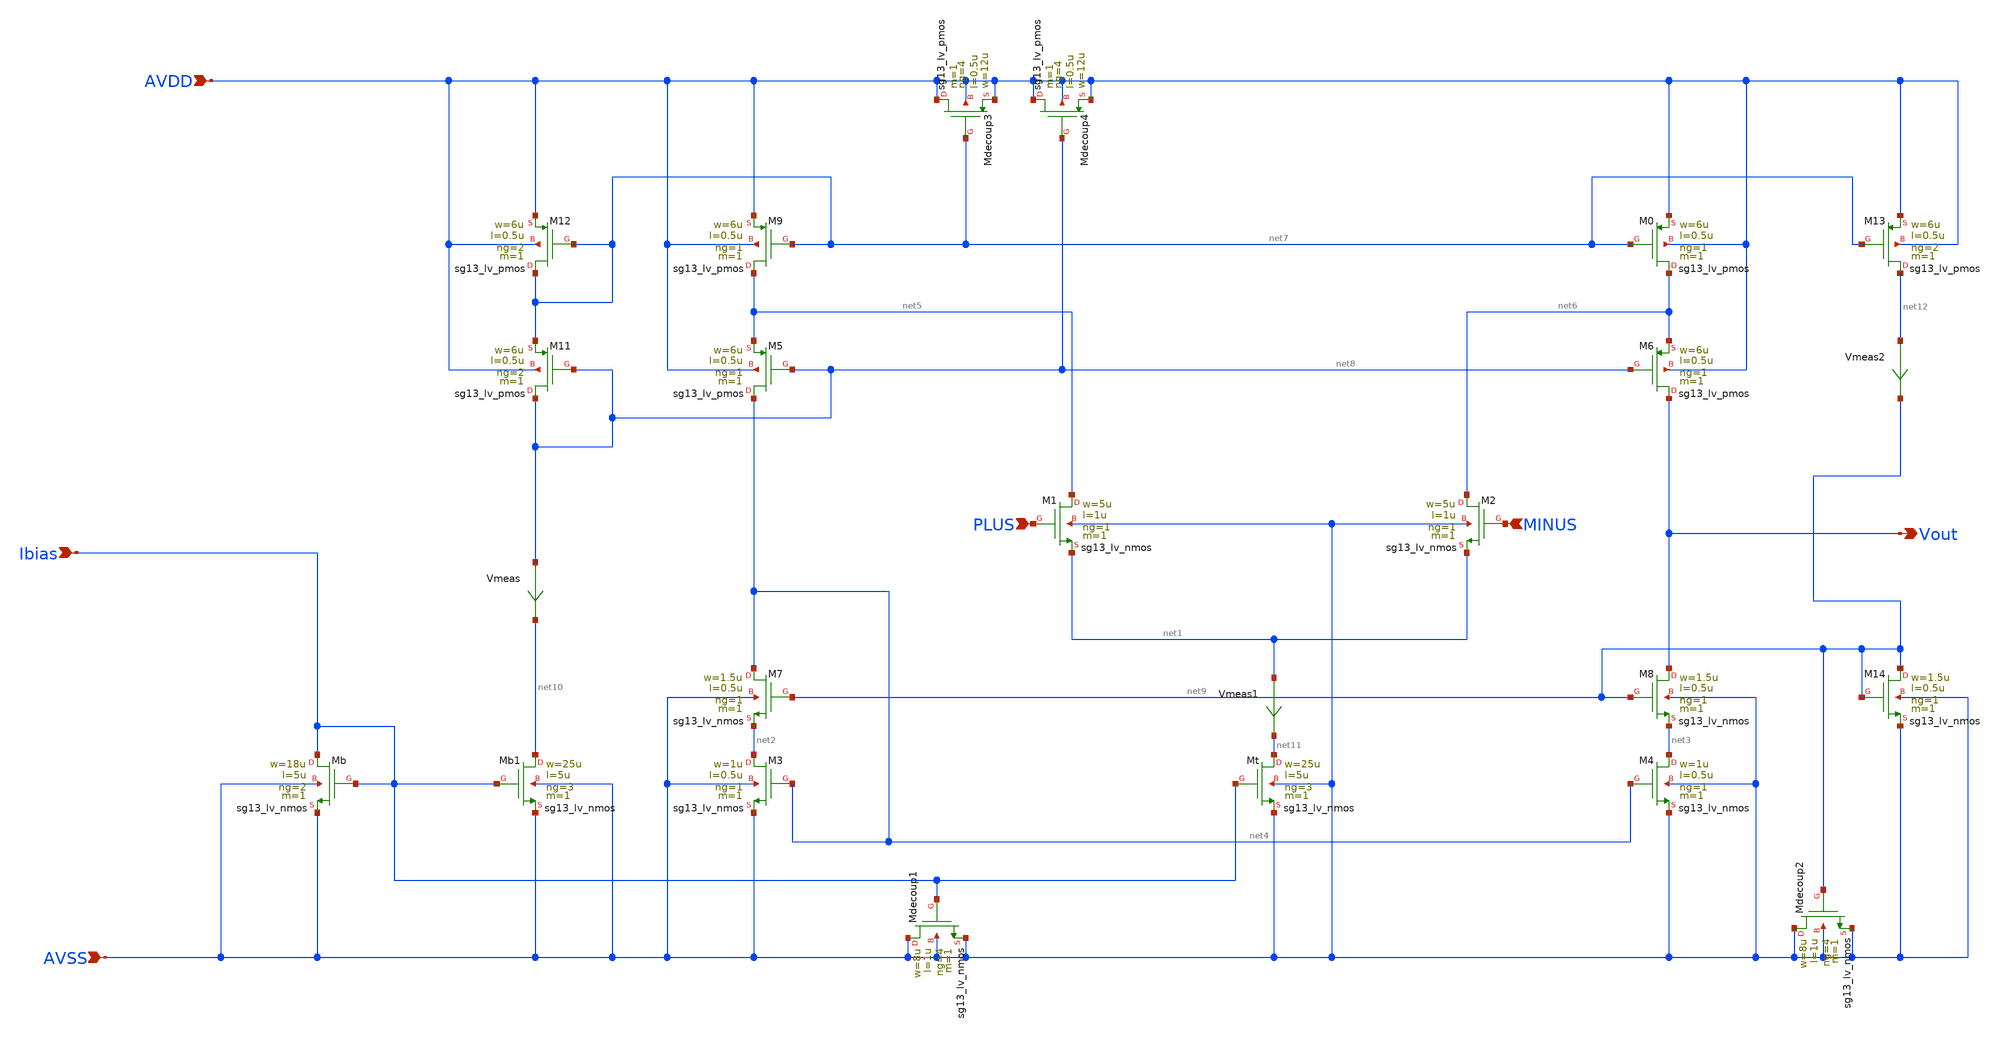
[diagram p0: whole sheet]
** sch_path: Designs/otas/foldedcascode_nmos.sch
* (c) 2025 Thesis_HP, Apache-2.0 license
**.subckt foldedcascode_nmos PLUS MINUS Vout AVDD AVSS Ibias
*.ipin PLUS
*.ipin MINUS
*.opin Vout
*.ipin AVDD
*.ipin AVSS
*.ipin Ibias
XM1 net5 PLUS net1 AVSS sg13_lv_nmos w=5u l=1u ng=1 m=1 mm_ok=1
XMt net11 Ibias AVSS AVSS sg13_lv_nmos w=25u l=5u ng=3 m=1 mm_ok=1
XM4 net3 net4 AVSS AVSS sg13_lv_nmos w=1u l=0.5u ng=1 m=1 mm_ok=1
XM3 net2 net4 AVSS AVSS sg13_lv_nmos w=1u l=0.5u ng=1 m=1 mm_ok=1
XM2 net6 MINUS net1 AVSS sg13_lv_nmos w=5u l=1u ng=1 m=1 mm_ok=1
XM7 net4 net9 net2 AVSS sg13_lv_nmos w=1.5u l=0.5u ng=1 m=1 mm_ok=1
XM8 Vout net9 net3 AVSS sg13_lv_nmos w=1.5u l=0.5u ng=1 m=1 mm_ok=1
XM5 net4 net8 net5 AVDD sg13_lv_pmos w=6u l=0.5u ng=1 m=1 mm_ok=1
XM9 net5 net7 AVDD AVDD sg13_lv_pmos w=6u l=0.5u ng=1 m=1 mm_ok=1
XM6 Vout net8 net6 AVDD sg13_lv_pmos w=6u l=0.5u ng=1 m=1 mm_ok=1
XM0 net6 net7 AVDD AVDD sg13_lv_pmos w=6u l=0.5u ng=1 m=1 mm_ok=1
XMb Ibias Ibias AVSS AVSS sg13_lv_nmos w=18u l=5u ng=2 m=1 mm_ok=1
XM11 net8 net8 net7 AVDD sg13_lv_pmos w=6u l=0.5u ng=2 m=1 mm_ok=1
XM12 net7 net7 AVDD AVDD sg13_lv_pmos w=6u l=0.5u ng=2 m=1 mm_ok=1
XM13 net12 net7 AVDD AVDD sg13_lv_pmos w=6u l=0.5u ng=2 m=1 mm_ok=1
XM14 net9 net9 AVSS AVSS sg13_lv_nmos w=1.5u l=0.5u ng=1 m=1 mm_ok=1
XMb1 net10 Ibias AVSS AVSS sg13_lv_nmos w=25u l=5u ng=3 m=1 mm_ok=1
Vmeas net8 net10 0
.save i(vmeas)
Vmeas1 net1 net11 0
.save i(vmeas1)
Vmeas2 net12 net9 0
.save i(vmeas2)
XMdecoup1 AVSS Ibias AVSS AVSS sg13_lv_nmos w=8u l=1u ng=4 m=1 mm_ok=1
XMdecoup2 AVSS net9 AVSS AVSS sg13_lv_nmos w=8u l=1u ng=4 m=1 mm_ok=1
XMdecoup3 AVDD net7 AVDD AVDD sg13_lv_pmos w=12u l=0.5u ng=4 m=1 mm_ok=1
XMdecoup4 AVDD net8 AVDD AVDD sg13_lv_pmos w=12u l=0.5u ng=4 m=1 mm_ok=1
**.ends
.end
